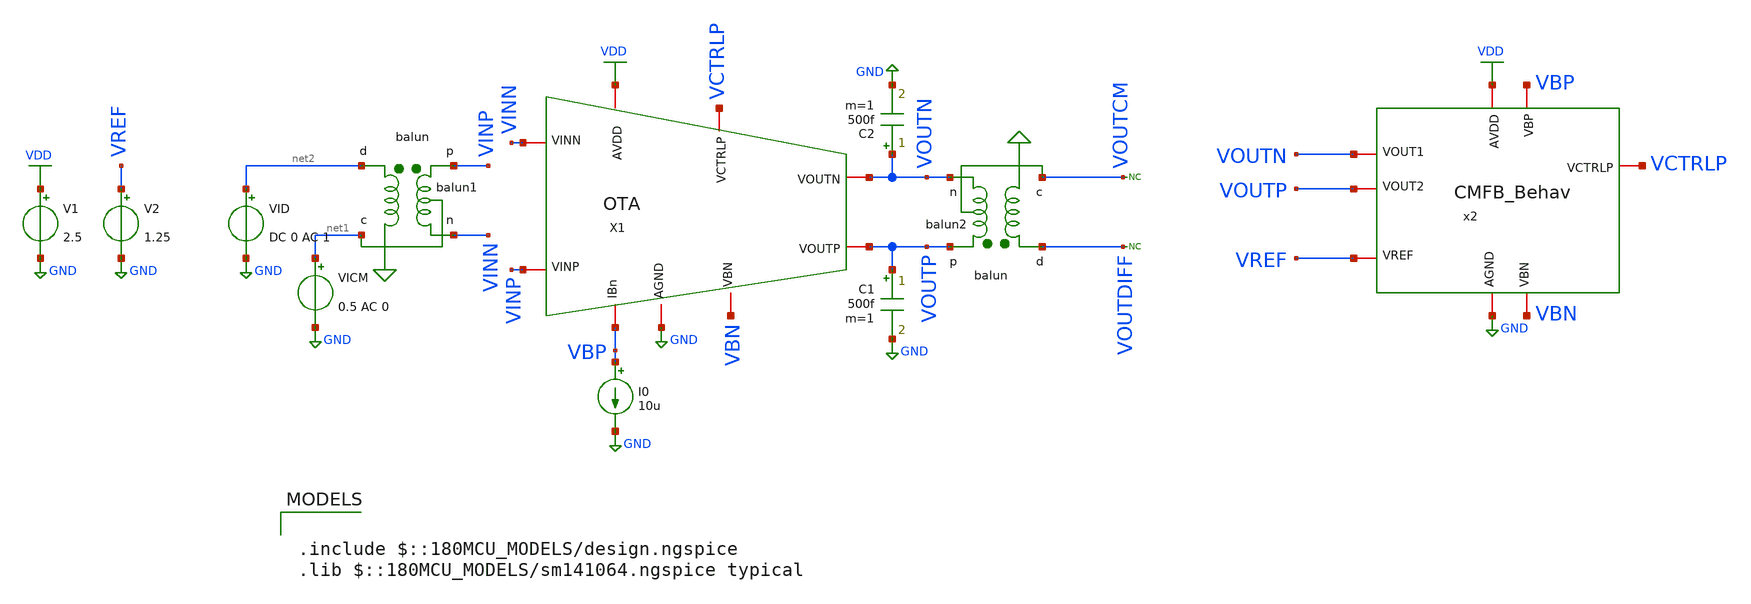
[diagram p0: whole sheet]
** sch_path: ITI_Labs/Lab11_Xschem/Design/Testbench.sch
**.subckt Testbench
X1 VDD VCTRLP VBP VOUTN VINP VOUTP VINN VBN GND OTA
Xbalun1 net2 net1 VINP VINN balun
V1 VDD GND 2.5
I0 VBP GND 10u
VICM net1 GND 0.5 AC 0
VID net2 GND DC 0 AC 1
C1 VOUTP GND 500f m=1
C2 VOUTN GND 500f m=1
Xbalun2 VOUTDIFF VOUTCM VOUTP VOUTN balun
x2 VDD GND VBN VOUTN VCTRLP VREF VBP VOUTP CMFB_Behav
V2 VREF GND 1.25
* noconn VOUTCM
* noconn VOUTDIFF
**** begin user architecture code


.include sim_script.sim



.include $::180MCU_MODELS/design.ngspice
.lib $::180MCU_MODELS/sm141064.ngspice typical

**** end user architecture code
**.ends
.GLOBAL VDD
.GLOBAL GND
.end
